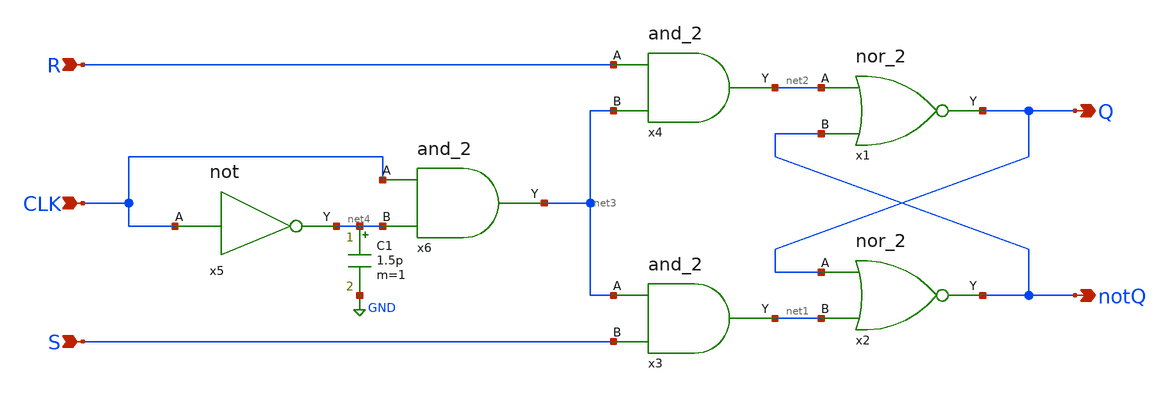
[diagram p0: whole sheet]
** sch_path: Circuiti/latches_sch_sym/sr_flip_flop.sch
**.subckt sr_flip_flop R S Q notQ CLK
*.ipin R
*.ipin S
*.opin Q
*.opin notQ
*.ipin CLK
x1 net2 Q notQ nor_2
x2 Q notQ net1 nor_2
x3 net3 net1 S and_2
x4 R net2 net3 and_2
x5 CLK net4 not
x6 CLK net3 net4 and_2
C1 net4 GND 1.5p m=1
**.ends

* expanding   symbol:  /home/matteo/Documenti/tesi/Circuiti/logic_gates_sch_sym/nor_2.sym # of
*+ pins=3
** sym_path: Circuiti/logic_gates_sch_sym/nor_2.sym
** sch_path: Circuiti/logic_gates_sch_sym/nor_2.sch
.subckt nor_2 A Y B
*.opin Y
*.ipin A
*.ipin B
XM1 Y B GND GND sky130_fd_pr__nfet_01v8 L=0.45 W=1 nf=1 ad='int((nf+1)/2) * W/nf * 0.29' as='int((nf+2)/2) * W/nf * 0.29'
+ pd='2*int((nf+1)/2) * (W/nf + 0.29)' ps='2*int((nf+2)/2) * (W/nf + 0.29)' nrd='0.29 / W' nrs='0.29 / W'
+ sa=0 sb=0 sd=0 mult=1 m=1
XM3 Y B net1 VDD sky130_fd_pr__pfet_01v8 L=0.15 W=4.8 nf=1 ad='int((nf+1)/2) * W/nf * 0.29' as='int((nf+2)/2) * W/nf * 0.29'
+ pd='2*int((nf+1)/2) * (W/nf + 0.29)' ps='2*int((nf+2)/2) * (W/nf + 0.29)' nrd='0.29 / W' nrs='0.29 / W'
+ sa=0 sb=0 sd=0 mult=1 m=1
XM4 net1 A Vdd VDD sky130_fd_pr__pfet_01v8 L=0.15 W=4.8 nf=1 ad='int((nf+1)/2) * W/nf * 0.29' as='int((nf+2)/2) * W/nf * 0.29'
+ pd='2*int((nf+1)/2) * (W/nf + 0.29)' ps='2*int((nf+2)/2) * (W/nf + 0.29)' nrd='0.29 / W' nrs='0.29 / W'
+ sa=0 sb=0 sd=0 mult=1 m=1
XM2 Y A GND GND sky130_fd_pr__nfet_01v8 L=0.45 W=1 nf=1 ad='int((nf+1)/2) * W/nf * 0.29' as='int((nf+2)/2) * W/nf * 0.29'
+ pd='2*int((nf+1)/2) * (W/nf + 0.29)' ps='2*int((nf+2)/2) * (W/nf + 0.29)' nrd='0.29 / W' nrs='0.29 / W'
+ sa=0 sb=0 sd=0 mult=1 m=1
.ends


* expanding   symbol:  /home/matteo/Documenti/tesi/Circuiti/logic_gates_sch_sym/and_2.sym # of
*+ pins=3
** sym_path: Circuiti/logic_gates_sch_sym/and_2.sym
** sch_path: Circuiti/logic_gates_sch_sym/and_2.sch
.subckt and_2 A Y B
*.ipin B
*.ipin A
*.opin Y
x1 A net1 B nand_2
x2 net1 Y not
.ends


* expanding   symbol:  /home/matteo/Documenti/tesi/Circuiti/logic_gates_sch_sym/not.sym # of pins=2
** sym_path: Circuiti/logic_gates_sch_sym/not.sym
** sch_path: Circuiti/logic_gates_sch_sym/not.sch
.subckt not A Y
*.ipin A
*.opin Y
XM1 Y A GND GND sky130_fd_pr__nfet_01v8 L=0.45 W=1 nf=1 ad='int((nf+1)/2) * W/nf * 0.29' as='int((nf+2)/2) * W/nf * 0.29'
+ pd='2*int((nf+1)/2) * (W/nf + 0.29)' ps='2*int((nf+2)/2) * (W/nf + 0.29)' nrd='0.29 / W' nrs='0.29 / W'
+ sa=0 sb=0 sd=0 mult=1 m=1
XM2 Y A Vdd VDD sky130_fd_pr__pfet_01v8 L=0.45 W=4.8 nf=1 ad='int((nf+1)/2) * W/nf * 0.29' as='int((nf+2)/2) * W/nf * 0.29'
+ pd='2*int((nf+1)/2) * (W/nf + 0.29)' ps='2*int((nf+2)/2) * (W/nf + 0.29)' nrd='0.29 / W' nrs='0.29 / W'
+ sa=0 sb=0 sd=0 mult=1 m=1
.ends


* expanding   symbol:  /home/matteo/Documenti/tesi/Circuiti/logic_gates_sch_sym/nand_2.sym # of
*+ pins=3
** sym_path: Circuiti/logic_gates_sch_sym/nand_2.sym
** sch_path: Circuiti/logic_gates_sch_sym/nand_2.sch
.subckt nand_2 A Y B
*.ipin A
*.ipin B
*.opin Y
XM1 Y A net1 GND sky130_fd_pr__nfet_01v8 L=0.15 W=1 nf=1 ad='int((nf+1)/2) * W/nf * 0.29' as='int((nf+2)/2) * W/nf * 0.29'
+ pd='2*int((nf+1)/2) * (W/nf + 0.29)' ps='2*int((nf+2)/2) * (W/nf + 0.29)' nrd='0.29 / W' nrs='0.29 / W'
+ sa=0 sb=0 sd=0 mult=1 m=1
XM3 Y B Vdd VDD sky130_fd_pr__pfet_01v8 L=0.45 W=4.8 nf=1 ad='int((nf+1)/2) * W/nf * 0.29' as='int((nf+2)/2) * W/nf * 0.29'
+ pd='2*int((nf+1)/2) * (W/nf + 0.29)' ps='2*int((nf+2)/2) * (W/nf + 0.29)' nrd='0.29 / W' nrs='0.29 / W'
+ sa=0 sb=0 sd=0 mult=1 m=1
XM4 Y A Vdd VDD sky130_fd_pr__pfet_01v8 L=0.45 W=4.8 nf=1 ad='int((nf+1)/2) * W/nf * 0.29' as='int((nf+2)/2) * W/nf * 0.29'
+ pd='2*int((nf+1)/2) * (W/nf + 0.29)' ps='2*int((nf+2)/2) * (W/nf + 0.29)' nrd='0.29 / W' nrs='0.29 / W'
+ sa=0 sb=0 sd=0 mult=1 m=1
XM2 net1 B GND GND sky130_fd_pr__nfet_01v8 L=0.15 W=1 nf=1 ad='int((nf+1)/2) * W/nf * 0.29' as='int((nf+2)/2) * W/nf * 0.29'
+ pd='2*int((nf+1)/2) * (W/nf + 0.29)' ps='2*int((nf+2)/2) * (W/nf + 0.29)' nrd='0.29 / W' nrs='0.29 / W'
+ sa=0 sb=0 sd=0 mult=1 m=1
.ends

.GLOBAL GND
.GLOBAL Vdd
.end
